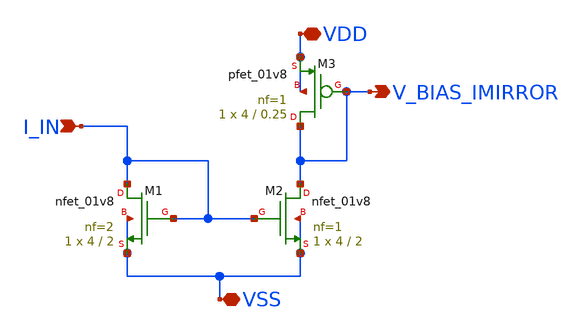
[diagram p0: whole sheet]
** sch_path: xschem/imirror_bias.sch
**.subckt imirror_bias VDD VSS V_BIAS_IMIRROR I_IN
*.iopin VDD
*.iopin VSS
*.opin V_BIAS_IMIRROR
*.ipin I_IN
XM1 I_IN I_IN VSS VSS sky130_fd_pr__nfet_01v8 L=2 W=4 nf=2 ad='int((nf+1)/2) * W/nf * 0.29' as='int((nf+2)/2) * W/nf * 0.29'
+ pd='2*int((nf+1)/2) * (W/nf + 0.29)' ps='2*int((nf+2)/2) * (W/nf + 0.29)' nrd='0.29 / W' nrs='0.29 / W'
+ sa=0 sb=0 sd=0 mult=1 m=1
XM2 V_BIAS_IMIRROR I_IN VSS VSS sky130_fd_pr__nfet_01v8 L=2 W=4 nf=1 ad='int((nf+1)/2) * W/nf * 0.29'
+ as='int((nf+2)/2) * W/nf * 0.29' pd='2*int((nf+1)/2) * (W/nf + 0.29)' ps='2*int((nf+2)/2) * (W/nf + 0.29)'
+ nrd='0.29 / W' nrs='0.29 / W' sa=0 sb=0 sd=0 mult=1 m=1
XM3 V_BIAS_IMIRROR V_BIAS_IMIRROR VDD VDD sky130_fd_pr__pfet_01v8 L=0.25 W=4 nf=1 ad='int((nf+1)/2) * W/nf * 0.29'
+ as='int((nf+2)/2) * W/nf * 0.29' pd='2*int((nf+1)/2) * (W/nf + 0.29)' ps='2*int((nf+2)/2) * (W/nf + 0.29)'
+ nrd='0.29 / W' nrs='0.29 / W' sa=0 sb=0 sd=0 mult=1 m=1
**.ends
.end
